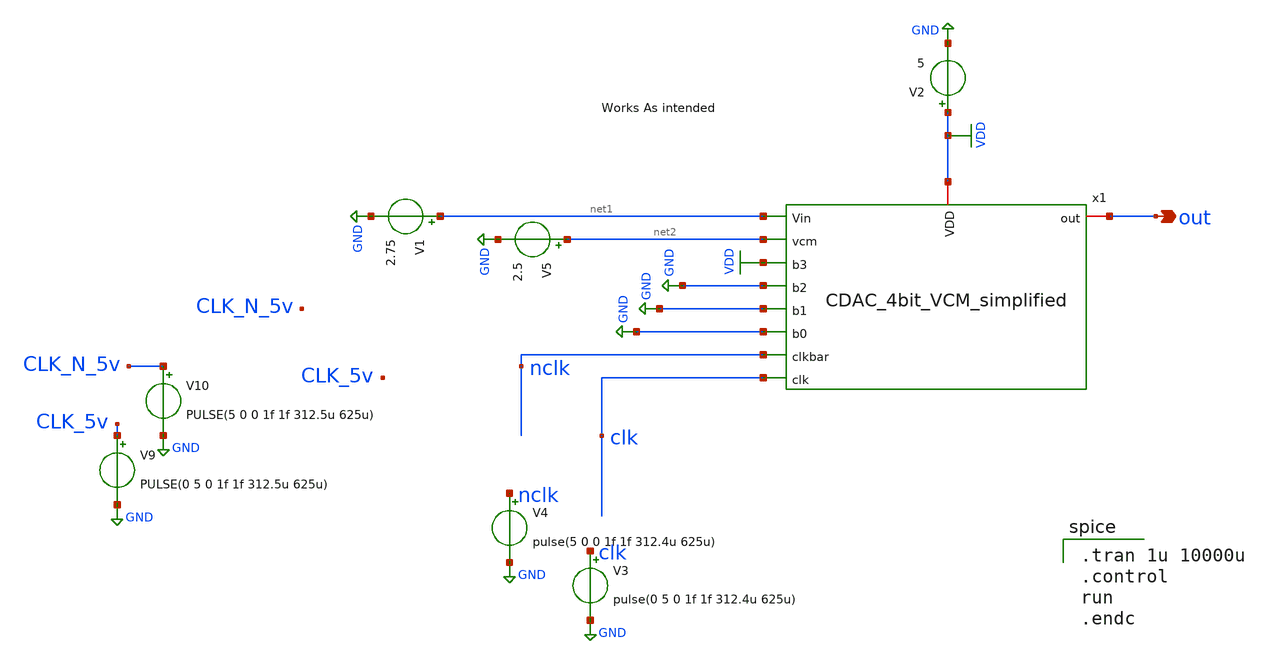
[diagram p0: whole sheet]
** sch_path: ADC/16bit_C2C/MagicAndSpice/CDAC_4bit_VCM_simplified_TB.sch
**.subckt CDAC_4bit_VCM_simplified_TB out
*.opin out
V2 VDD GND 5
V3 clk GND pulse(0 5 0 1f 1f 312.4u 625u)
V4 nclk GND pulse(5 0 0 1f 1f 312.4u 625u)
V1 net1 GND 2.75
V5 net2 GND 2.5
x1 nclk clk net1 VDD GND GND GND net2 out VDD CDAC_4bit_VCM_simplified
V9 CLK_5v GND PULSE(0 5 0 1f 1f 312.5u 625u)
V10 CLK_N_5v GND PULSE(5 0 0 1f 1f 312.5u 625u)
**** begin user architecture code

** opencircuitdesign pdks install
.lib $::SKYWATER_MODELS/sky130.lib.spice tt



.tran 1u 10000u
.control
run
.endc

**** end user architecture code
**.ends
.GLOBAL GND
.GLOBAL VDD
.end
